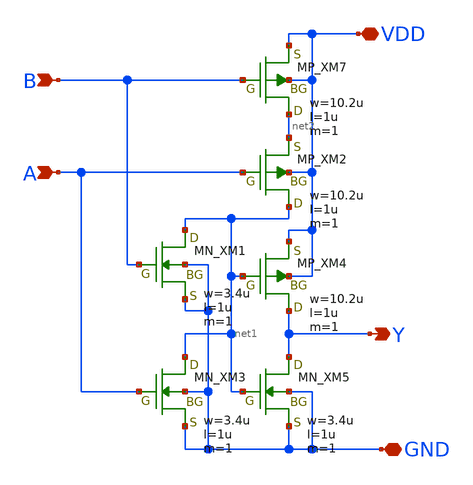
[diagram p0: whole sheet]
** sch_path: openIP62_rev1.0/IP62/Technology/tech/symbols/Xschem/IP62_5_stdcell/OR2.sch
**.subckt OR2 A B Y VDD GND
*.ipin A
*.ipin B
*.opin Y
*.iopin VDD
*.iopin GND
XM7 net2 B VDD VDD PMOS w=10.2u l=1u as=0 ad=0 ps=0 pd=0 nrd=0 nrs=0 m=1
XM2 net1 A net2 VDD PMOS w=10.2u l=1u as=0 ad=0 ps=0 pd=0 nrd=0 nrs=0 m=1
XM4 Y net1 VDD VDD PMOS w=10.2u l=1u as=0 ad=0 ps=0 pd=0 nrd=0 nrs=0 m=1
XM1 net1 B GND GND NMOS w=3.4u l=1u as=0 ad=0 ps=0 pd=0 nrd=0 nrs=0 m=1
XM3 net1 A GND GND NMOS w=3.4u l=1u as=0 ad=0 ps=0 pd=0 nrd=0 nrs=0 m=1
XM5 Y net1 GND GND NMOS w=3.4u l=1u as=0 ad=0 ps=0 pd=0 nrd=0 nrs=0 m=1
**.ends
.end
